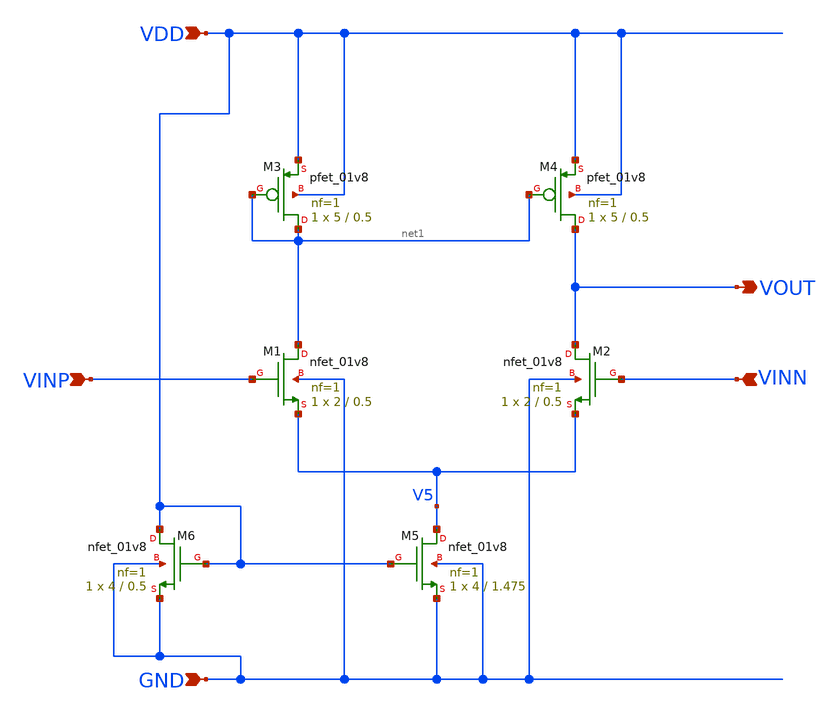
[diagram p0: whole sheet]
** sch_path: xschem/ota_5t_sky130.sch
**.subckt ota_5t_sky130 VINP VINN VOUT VDD GND
*.ipin VINP
*.ipin VINN
*.opin VOUT
*.ipin VDD
*.ipin GND
XM5 V5 VDD GND GND sky130_fd_pr__nfet_01v8 L=1.475 W=4 nf=1 ad='int((1 + 1)/2) * 4 / 1 * 0.29' as='int((1 + 2)/2) * 4 / 1 * 0.29'
+ pd='2*int((1 + 1)/2) * (4 / 1 + 0.29)' ps='2*int((1 + 2)/2) * (4 / 1 + 0.29)' nrd='0.29 / 4 ' nrs='0.29 / 4 '
+ sa=0 sb=0 sd=0 mult=1 m=1
XM1 net1 VINP V5 GND sky130_fd_pr__nfet_01v8 L=0.5 W=2 nf=1 ad='int((1 + 1)/2) * 2 / 1 * 0.29' as='int((1 + 2)/2) * 2 / 1 * 0.29'
+ pd='2*int((1 + 1)/2) * (2 / 1 + 0.29)' ps='2*int((1 + 2)/2) * (2 / 1 + 0.29)' nrd='0.29 / 2 ' nrs='0.29 / 2 '
+ sa=0 sb=0 sd=0 mult=1 m=1
XM2 VOUT VINN V5 GND sky130_fd_pr__nfet_01v8 L=0.5 W=2 nf=1 ad='int((1 + 1)/2) * 2 / 1 * 0.29' as='int((1 + 2)/2) * 2 / 1 * 0.29'
+ pd='2*int((1 + 1)/2) * (2 / 1 + 0.29)' ps='2*int((1 + 2)/2) * (2 / 1 + 0.29)' nrd='0.29 / 2 ' nrs='0.29 / 2 '
+ sa=0 sb=0 sd=0 mult=1 m=1
XM3 net1 net1 VDD VDD sky130_fd_pr__pfet_01v8 L=0.5 W=5 nf=1 ad='int((1 + 1)/2) * 5 / 1 * 0.29' as='int((1 + 2)/2) * 5 / 1 * 0.29'
+ pd='2*int((1 + 1)/2) * (5 / 1 + 0.29)' ps='2*int((1 + 2)/2) * (5 / 1 + 0.29)' nrd='0.29 / 5 ' nrs='0.29 / 5 '
+ sa=0 sb=0 sd=0 mult=1 m=1
XM4 VOUT net1 VDD VDD sky130_fd_pr__pfet_01v8 L=0.5 W=5 nf=1 ad='int((1 + 1)/2) * 5 / 1 * 0.29' as='int((1 + 2)/2) * 5 / 1 * 0.29'
+ pd='2*int((1 + 1)/2) * (5 / 1 + 0.29)' ps='2*int((1 + 2)/2) * (5 / 1 + 0.29)' nrd='0.29 / 5 ' nrs='0.29 / 5 '
+ sa=0 sb=0 sd=0 mult=1 m=1
XM6 VDD VDD GND GND sky130_fd_pr__nfet_01v8 L=0.5 W=4 nf=1 ad='int((1 + 1)/2) * 4 / 1 * 0.29' as='int((1 + 2)/2) * 4 / 1 * 0.29'
+ pd='2*int((1 + 1)/2) * (4 / 1 + 0.29)' ps='2*int((1 + 2)/2) * (4 / 1 + 0.29)' nrd='0.29 / 4 ' nrs='0.29 / 4 '
+ sa=0 sb=0 sd=0 mult=1 m=1
**.ends
.end
